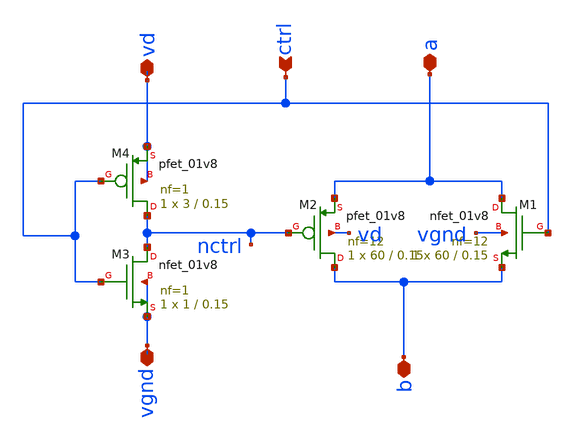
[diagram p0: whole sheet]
** sch_path: xschem/tg.sch
**.subckt tg vd vgnd b a ctrl
*.iopin vd
*.iopin vgnd
*.iopin b
*.iopin a
*.ipin ctrl
XM2 b nctrl a vd sky130_fd_pr__pfet_01v8 L=0.15 W=60 nf=12 ad='int((nf+1)/2) * W/nf * 0.29' as='int((nf+2)/2) * W/nf * 0.29'
+ pd='2*int((nf+1)/2) * (W/nf + 0.29)' ps='2*int((nf+2)/2) * (W/nf + 0.29)' nrd='0.29 / W' nrs='0.29 / W'
+ sa=0 sb=0 sd=0 mult=1 m=1
XM1 a ctrl b vgnd sky130_fd_pr__nfet_01v8 L=0.15 W=60 nf=12 ad='int((nf+1)/2) * W/nf * 0.29' as='int((nf+2)/2) * W/nf * 0.29'
+ pd='2*int((nf+1)/2) * (W/nf + 0.29)' ps='2*int((nf+2)/2) * (W/nf + 0.29)' nrd='0.29 / W' nrs='0.29 / W'
+ sa=0 sb=0 sd=0 mult=1 m=1
XM3 nctrl ctrl vgnd vgnd sky130_fd_pr__nfet_01v8 L=0.15 W=1 nf=1 ad='int((nf+1)/2) * W/nf * 0.29' as='int((nf+2)/2) * W/nf * 0.29'
+ pd='2*int((nf+1)/2) * (W/nf + 0.29)' ps='2*int((nf+2)/2) * (W/nf + 0.29)' nrd='0.29 / W' nrs='0.29 / W'
+ sa=0 sb=0 sd=0 mult=1 m=1
XM4 nctrl ctrl vd vd sky130_fd_pr__pfet_01v8 L=0.15 W=3 nf=1 ad='int((nf+1)/2) * W/nf * 0.29' as='int((nf+2)/2) * W/nf * 0.29'
+ pd='2*int((nf+1)/2) * (W/nf + 0.29)' ps='2*int((nf+2)/2) * (W/nf + 0.29)' nrd='0.29 / W' nrs='0.29 / W'
+ sa=0 sb=0 sd=0 mult=1 m=1
**.ends
.end
